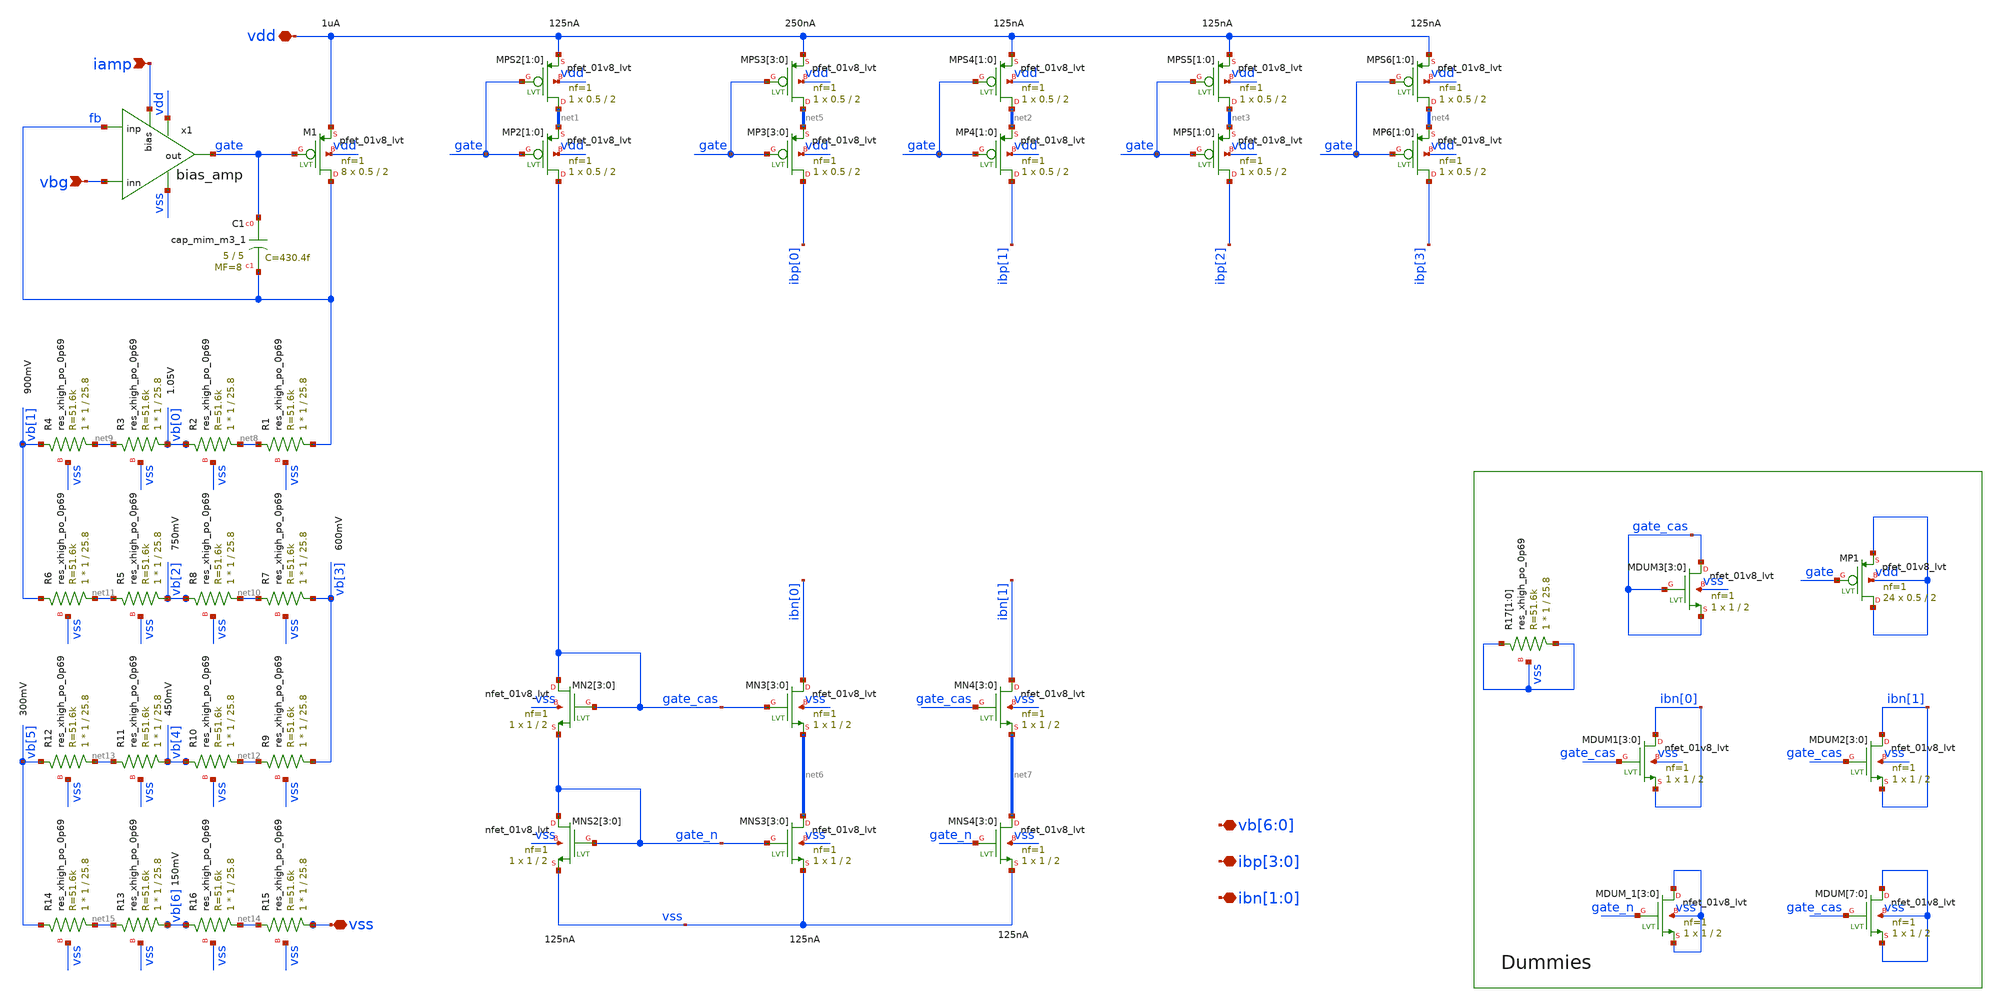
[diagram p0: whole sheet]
** sch_path: xschem/bias/bias.sch
**.subckt bias vbg iamp vdd ibp[3],ibp[2],ibp[1],ibp[0] ibn[1],ibn[0]
*+ vb[6],vb[5],vb[4],vb[3],vb[2],vb[1],vb[0] vss
*.ipin vbg
*.ipin iamp
*.iopin vdd
*.iopin ibp[3],ibp[2],ibp[1],ibp[0]
*.iopin ibn[1],ibn[0]
*.iopin vb[6],vb[5],vb[4],vb[3],vb[2],vb[1],vb[0]
*.iopin vss
x1 vdd gate fb vbg vss iamp bias_amp
XMP2[1] gate_cas gate net1[1] vdd sky130_fd_pr__pfet_01v8_lvt L=2 W=0.5 nf=1 ad='int((nf+1)/2) * W/nf * 0.29'
+ as='int((nf+2)/2) * W/nf * 0.29' pd='2*int((nf+1)/2) * (W/nf + 0.29)' ps='2*int((nf+2)/2) * (W/nf + 0.29)'
+ nrd='0.29 / W' nrs='0.29 / W' sa=0 sb=0 sd=0 mult=1 m=1
XMP2[0] gate_cas gate net1[0] vdd sky130_fd_pr__pfet_01v8_lvt L=2 W=0.5 nf=1 ad='int((nf+1)/2) * W/nf * 0.29'
+ as='int((nf+2)/2) * W/nf * 0.29' pd='2*int((nf+1)/2) * (W/nf + 0.29)' ps='2*int((nf+2)/2) * (W/nf + 0.29)'
+ nrd='0.29 / W' nrs='0.29 / W' sa=0 sb=0 sd=0 mult=1 m=1
XM1 fb gate vdd vdd sky130_fd_pr__pfet_01v8_lvt L=2 W=0.5 nf=1 ad='int((nf+1)/2) * W/nf * 0.29' as='int((nf+2)/2) * W/nf * 0.29'
+ pd='2*int((nf+1)/2) * (W/nf + 0.29)' ps='2*int((nf+2)/2) * (W/nf + 0.29)' nrd='0.29 / W' nrs='0.29 / W'
+ sa=0 sb=0 sd=0 mult=8 m=8
XMPS2[1] net1[1] gate vdd vdd sky130_fd_pr__pfet_01v8_lvt L=2 W=0.5 nf=1 ad='int((nf+1)/2) * W/nf * 0.29'
+ as='int((nf+2)/2) * W/nf * 0.29' pd='2*int((nf+1)/2) * (W/nf + 0.29)' ps='2*int((nf+2)/2) * (W/nf + 0.29)'
+ nrd='0.29 / W' nrs='0.29 / W' sa=0 sb=0 sd=0 mult=1 m=1
XMPS2[0] net1[0] gate vdd vdd sky130_fd_pr__pfet_01v8_lvt L=2 W=0.5 nf=1 ad='int((nf+1)/2) * W/nf * 0.29'
+ as='int((nf+2)/2) * W/nf * 0.29' pd='2*int((nf+1)/2) * (W/nf + 0.29)' ps='2*int((nf+2)/2) * (W/nf + 0.29)'
+ nrd='0.29 / W' nrs='0.29 / W' sa=0 sb=0 sd=0 mult=1 m=1
XMP4[1] ibp[1] gate net2[1] vdd sky130_fd_pr__pfet_01v8_lvt L=2 W=0.5 nf=1 ad='int((nf+1)/2) * W/nf * 0.29'
+ as='int((nf+2)/2) * W/nf * 0.29' pd='2*int((nf+1)/2) * (W/nf + 0.29)' ps='2*int((nf+2)/2) * (W/nf + 0.29)'
+ nrd='0.29 / W' nrs='0.29 / W' sa=0 sb=0 sd=0 mult=1 m=1
XMP4[0] ibp[1] gate net2[0] vdd sky130_fd_pr__pfet_01v8_lvt L=2 W=0.5 nf=1 ad='int((nf+1)/2) * W/nf * 0.29'
+ as='int((nf+2)/2) * W/nf * 0.29' pd='2*int((nf+1)/2) * (W/nf + 0.29)' ps='2*int((nf+2)/2) * (W/nf + 0.29)'
+ nrd='0.29 / W' nrs='0.29 / W' sa=0 sb=0 sd=0 mult=1 m=1
XMPS4[1] net2[1] gate vdd vdd sky130_fd_pr__pfet_01v8_lvt L=2 W=0.5 nf=1 ad='int((nf+1)/2) * W/nf * 0.29'
+ as='int((nf+2)/2) * W/nf * 0.29' pd='2*int((nf+1)/2) * (W/nf + 0.29)' ps='2*int((nf+2)/2) * (W/nf + 0.29)'
+ nrd='0.29 / W' nrs='0.29 / W' sa=0 sb=0 sd=0 mult=1 m=1
XMPS4[0] net2[0] gate vdd vdd sky130_fd_pr__pfet_01v8_lvt L=2 W=0.5 nf=1 ad='int((nf+1)/2) * W/nf * 0.29'
+ as='int((nf+2)/2) * W/nf * 0.29' pd='2*int((nf+1)/2) * (W/nf + 0.29)' ps='2*int((nf+2)/2) * (W/nf + 0.29)'
+ nrd='0.29 / W' nrs='0.29 / W' sa=0 sb=0 sd=0 mult=1 m=1
XMP5[1] ibp[2] gate net3[1] vdd sky130_fd_pr__pfet_01v8_lvt L=2 W=0.5 nf=1 ad='int((nf+1)/2) * W/nf * 0.29'
+ as='int((nf+2)/2) * W/nf * 0.29' pd='2*int((nf+1)/2) * (W/nf + 0.29)' ps='2*int((nf+2)/2) * (W/nf + 0.29)'
+ nrd='0.29 / W' nrs='0.29 / W' sa=0 sb=0 sd=0 mult=1 m=1
XMP5[0] ibp[2] gate net3[0] vdd sky130_fd_pr__pfet_01v8_lvt L=2 W=0.5 nf=1 ad='int((nf+1)/2) * W/nf * 0.29'
+ as='int((nf+2)/2) * W/nf * 0.29' pd='2*int((nf+1)/2) * (W/nf + 0.29)' ps='2*int((nf+2)/2) * (W/nf + 0.29)'
+ nrd='0.29 / W' nrs='0.29 / W' sa=0 sb=0 sd=0 mult=1 m=1
XMPS5[1] net3[1] gate vdd vdd sky130_fd_pr__pfet_01v8_lvt L=2 W=0.5 nf=1 ad='int((nf+1)/2) * W/nf * 0.29'
+ as='int((nf+2)/2) * W/nf * 0.29' pd='2*int((nf+1)/2) * (W/nf + 0.29)' ps='2*int((nf+2)/2) * (W/nf + 0.29)'
+ nrd='0.29 / W' nrs='0.29 / W' sa=0 sb=0 sd=0 mult=1 m=1
XMPS5[0] net3[0] gate vdd vdd sky130_fd_pr__pfet_01v8_lvt L=2 W=0.5 nf=1 ad='int((nf+1)/2) * W/nf * 0.29'
+ as='int((nf+2)/2) * W/nf * 0.29' pd='2*int((nf+1)/2) * (W/nf + 0.29)' ps='2*int((nf+2)/2) * (W/nf + 0.29)'
+ nrd='0.29 / W' nrs='0.29 / W' sa=0 sb=0 sd=0 mult=1 m=1
XMP6[1] ibp[3] gate net4[1] vdd sky130_fd_pr__pfet_01v8_lvt L=2 W=0.5 nf=1 ad='int((nf+1)/2) * W/nf * 0.29'
+ as='int((nf+2)/2) * W/nf * 0.29' pd='2*int((nf+1)/2) * (W/nf + 0.29)' ps='2*int((nf+2)/2) * (W/nf + 0.29)'
+ nrd='0.29 / W' nrs='0.29 / W' sa=0 sb=0 sd=0 mult=1 m=1
XMP6[0] ibp[3] gate net4[0] vdd sky130_fd_pr__pfet_01v8_lvt L=2 W=0.5 nf=1 ad='int((nf+1)/2) * W/nf * 0.29'
+ as='int((nf+2)/2) * W/nf * 0.29' pd='2*int((nf+1)/2) * (W/nf + 0.29)' ps='2*int((nf+2)/2) * (W/nf + 0.29)'
+ nrd='0.29 / W' nrs='0.29 / W' sa=0 sb=0 sd=0 mult=1 m=1
XMPS6[1] net4[1] gate vdd vdd sky130_fd_pr__pfet_01v8_lvt L=2 W=0.5 nf=1 ad='int((nf+1)/2) * W/nf * 0.29'
+ as='int((nf+2)/2) * W/nf * 0.29' pd='2*int((nf+1)/2) * (W/nf + 0.29)' ps='2*int((nf+2)/2) * (W/nf + 0.29)'
+ nrd='0.29 / W' nrs='0.29 / W' sa=0 sb=0 sd=0 mult=1 m=1
XMPS6[0] net4[0] gate vdd vdd sky130_fd_pr__pfet_01v8_lvt L=2 W=0.5 nf=1 ad='int((nf+1)/2) * W/nf * 0.29'
+ as='int((nf+2)/2) * W/nf * 0.29' pd='2*int((nf+1)/2) * (W/nf + 0.29)' ps='2*int((nf+2)/2) * (W/nf + 0.29)'
+ nrd='0.29 / W' nrs='0.29 / W' sa=0 sb=0 sd=0 mult=1 m=1
XMP3[3] ibp[0] gate net5[3] vdd sky130_fd_pr__pfet_01v8_lvt L=2 W=0.5 nf=1 ad='int((nf+1)/2) * W/nf * 0.29'
+ as='int((nf+2)/2) * W/nf * 0.29' pd='2*int((nf+1)/2) * (W/nf + 0.29)' ps='2*int((nf+2)/2) * (W/nf + 0.29)'
+ nrd='0.29 / W' nrs='0.29 / W' sa=0 sb=0 sd=0 mult=1 m=1
XMP3[2] ibp[0] gate net5[2] vdd sky130_fd_pr__pfet_01v8_lvt L=2 W=0.5 nf=1 ad='int((nf+1)/2) * W/nf * 0.29'
+ as='int((nf+2)/2) * W/nf * 0.29' pd='2*int((nf+1)/2) * (W/nf + 0.29)' ps='2*int((nf+2)/2) * (W/nf + 0.29)'
+ nrd='0.29 / W' nrs='0.29 / W' sa=0 sb=0 sd=0 mult=1 m=1
XMP3[1] ibp[0] gate net5[1] vdd sky130_fd_pr__pfet_01v8_lvt L=2 W=0.5 nf=1 ad='int((nf+1)/2) * W/nf * 0.29'
+ as='int((nf+2)/2) * W/nf * 0.29' pd='2*int((nf+1)/2) * (W/nf + 0.29)' ps='2*int((nf+2)/2) * (W/nf + 0.29)'
+ nrd='0.29 / W' nrs='0.29 / W' sa=0 sb=0 sd=0 mult=1 m=1
XMP3[0] ibp[0] gate net5[0] vdd sky130_fd_pr__pfet_01v8_lvt L=2 W=0.5 nf=1 ad='int((nf+1)/2) * W/nf * 0.29'
+ as='int((nf+2)/2) * W/nf * 0.29' pd='2*int((nf+1)/2) * (W/nf + 0.29)' ps='2*int((nf+2)/2) * (W/nf + 0.29)'
+ nrd='0.29 / W' nrs='0.29 / W' sa=0 sb=0 sd=0 mult=1 m=1
XMPS3[3] net5[3] gate vdd vdd sky130_fd_pr__pfet_01v8_lvt L=2 W=0.5 nf=1 ad='int((nf+1)/2) * W/nf * 0.29'
+ as='int((nf+2)/2) * W/nf * 0.29' pd='2*int((nf+1)/2) * (W/nf + 0.29)' ps='2*int((nf+2)/2) * (W/nf + 0.29)'
+ nrd='0.29 / W' nrs='0.29 / W' sa=0 sb=0 sd=0 mult=1 m=1
XMPS3[2] net5[2] gate vdd vdd sky130_fd_pr__pfet_01v8_lvt L=2 W=0.5 nf=1 ad='int((nf+1)/2) * W/nf * 0.29'
+ as='int((nf+2)/2) * W/nf * 0.29' pd='2*int((nf+1)/2) * (W/nf + 0.29)' ps='2*int((nf+2)/2) * (W/nf + 0.29)'
+ nrd='0.29 / W' nrs='0.29 / W' sa=0 sb=0 sd=0 mult=1 m=1
XMPS3[1] net5[1] gate vdd vdd sky130_fd_pr__pfet_01v8_lvt L=2 W=0.5 nf=1 ad='int((nf+1)/2) * W/nf * 0.29'
+ as='int((nf+2)/2) * W/nf * 0.29' pd='2*int((nf+1)/2) * (W/nf + 0.29)' ps='2*int((nf+2)/2) * (W/nf + 0.29)'
+ nrd='0.29 / W' nrs='0.29 / W' sa=0 sb=0 sd=0 mult=1 m=1
XMPS3[0] net5[0] gate vdd vdd sky130_fd_pr__pfet_01v8_lvt L=2 W=0.5 nf=1 ad='int((nf+1)/2) * W/nf * 0.29'
+ as='int((nf+2)/2) * W/nf * 0.29' pd='2*int((nf+1)/2) * (W/nf + 0.29)' ps='2*int((nf+2)/2) * (W/nf + 0.29)'
+ nrd='0.29 / W' nrs='0.29 / W' sa=0 sb=0 sd=0 mult=1 m=1
XMNS2[3] gate_n gate_n vss vss sky130_fd_pr__nfet_01v8_lvt L=2 W=1 nf=1 ad='int((nf+1)/2) * W/nf * 0.29'
+ as='int((nf+2)/2) * W/nf * 0.29' pd='2*int((nf+1)/2) * (W/nf + 0.29)' ps='2*int((nf+2)/2) * (W/nf + 0.29)'
+ nrd='0.29 / W' nrs='0.29 / W' sa=0 sb=0 sd=0 mult=1 m=1
XMNS2[2] gate_n gate_n vss vss sky130_fd_pr__nfet_01v8_lvt L=2 W=1 nf=1 ad='int((nf+1)/2) * W/nf * 0.29'
+ as='int((nf+2)/2) * W/nf * 0.29' pd='2*int((nf+1)/2) * (W/nf + 0.29)' ps='2*int((nf+2)/2) * (W/nf + 0.29)'
+ nrd='0.29 / W' nrs='0.29 / W' sa=0 sb=0 sd=0 mult=1 m=1
XMNS2[1] gate_n gate_n vss vss sky130_fd_pr__nfet_01v8_lvt L=2 W=1 nf=1 ad='int((nf+1)/2) * W/nf * 0.29'
+ as='int((nf+2)/2) * W/nf * 0.29' pd='2*int((nf+1)/2) * (W/nf + 0.29)' ps='2*int((nf+2)/2) * (W/nf + 0.29)'
+ nrd='0.29 / W' nrs='0.29 / W' sa=0 sb=0 sd=0 mult=1 m=1
XMNS2[0] gate_n gate_n vss vss sky130_fd_pr__nfet_01v8_lvt L=2 W=1 nf=1 ad='int((nf+1)/2) * W/nf * 0.29'
+ as='int((nf+2)/2) * W/nf * 0.29' pd='2*int((nf+1)/2) * (W/nf + 0.29)' ps='2*int((nf+2)/2) * (W/nf + 0.29)'
+ nrd='0.29 / W' nrs='0.29 / W' sa=0 sb=0 sd=0 mult=1 m=1
XMNS3[3] net6[3] gate_n vss vss sky130_fd_pr__nfet_01v8_lvt L=2 W=1 nf=1 ad='int((nf+1)/2) * W/nf * 0.29'
+ as='int((nf+2)/2) * W/nf * 0.29' pd='2*int((nf+1)/2) * (W/nf + 0.29)' ps='2*int((nf+2)/2) * (W/nf + 0.29)'
+ nrd='0.29 / W' nrs='0.29 / W' sa=0 sb=0 sd=0 mult=1 m=1
XMNS3[2] net6[2] gate_n vss vss sky130_fd_pr__nfet_01v8_lvt L=2 W=1 nf=1 ad='int((nf+1)/2) * W/nf * 0.29'
+ as='int((nf+2)/2) * W/nf * 0.29' pd='2*int((nf+1)/2) * (W/nf + 0.29)' ps='2*int((nf+2)/2) * (W/nf + 0.29)'
+ nrd='0.29 / W' nrs='0.29 / W' sa=0 sb=0 sd=0 mult=1 m=1
XMNS3[1] net6[1] gate_n vss vss sky130_fd_pr__nfet_01v8_lvt L=2 W=1 nf=1 ad='int((nf+1)/2) * W/nf * 0.29'
+ as='int((nf+2)/2) * W/nf * 0.29' pd='2*int((nf+1)/2) * (W/nf + 0.29)' ps='2*int((nf+2)/2) * (W/nf + 0.29)'
+ nrd='0.29 / W' nrs='0.29 / W' sa=0 sb=0 sd=0 mult=1 m=1
XMNS3[0] net6[0] gate_n vss vss sky130_fd_pr__nfet_01v8_lvt L=2 W=1 nf=1 ad='int((nf+1)/2) * W/nf * 0.29'
+ as='int((nf+2)/2) * W/nf * 0.29' pd='2*int((nf+1)/2) * (W/nf + 0.29)' ps='2*int((nf+2)/2) * (W/nf + 0.29)'
+ nrd='0.29 / W' nrs='0.29 / W' sa=0 sb=0 sd=0 mult=1 m=1
XMNS4[3] net7[3] gate_n vss vss sky130_fd_pr__nfet_01v8_lvt L=2 W=1 nf=1 ad='int((nf+1)/2) * W/nf * 0.29'
+ as='int((nf+2)/2) * W/nf * 0.29' pd='2*int((nf+1)/2) * (W/nf + 0.29)' ps='2*int((nf+2)/2) * (W/nf + 0.29)'
+ nrd='0.29 / W' nrs='0.29 / W' sa=0 sb=0 sd=0 mult=1 m=1
XMNS4[2] net7[2] gate_n vss vss sky130_fd_pr__nfet_01v8_lvt L=2 W=1 nf=1 ad='int((nf+1)/2) * W/nf * 0.29'
+ as='int((nf+2)/2) * W/nf * 0.29' pd='2*int((nf+1)/2) * (W/nf + 0.29)' ps='2*int((nf+2)/2) * (W/nf + 0.29)'
+ nrd='0.29 / W' nrs='0.29 / W' sa=0 sb=0 sd=0 mult=1 m=1
XMNS4[1] net7[1] gate_n vss vss sky130_fd_pr__nfet_01v8_lvt L=2 W=1 nf=1 ad='int((nf+1)/2) * W/nf * 0.29'
+ as='int((nf+2)/2) * W/nf * 0.29' pd='2*int((nf+1)/2) * (W/nf + 0.29)' ps='2*int((nf+2)/2) * (W/nf + 0.29)'
+ nrd='0.29 / W' nrs='0.29 / W' sa=0 sb=0 sd=0 mult=1 m=1
XMNS4[0] net7[0] gate_n vss vss sky130_fd_pr__nfet_01v8_lvt L=2 W=1 nf=1 ad='int((nf+1)/2) * W/nf * 0.29'
+ as='int((nf+2)/2) * W/nf * 0.29' pd='2*int((nf+1)/2) * (W/nf + 0.29)' ps='2*int((nf+2)/2) * (W/nf + 0.29)'
+ nrd='0.29 / W' nrs='0.29 / W' sa=0 sb=0 sd=0 mult=1 m=1
XMN2[3] gate_cas gate_cas gate_n vss sky130_fd_pr__nfet_01v8_lvt L=2 W=1 nf=1 ad='int((nf+1)/2) * W/nf * 0.29'
+ as='int((nf+2)/2) * W/nf * 0.29' pd='2*int((nf+1)/2) * (W/nf + 0.29)' ps='2*int((nf+2)/2) * (W/nf + 0.29)'
+ nrd='0.29 / W' nrs='0.29 / W' sa=0 sb=0 sd=0 mult=1 m=1
XMN2[2] gate_cas gate_cas gate_n vss sky130_fd_pr__nfet_01v8_lvt L=2 W=1 nf=1 ad='int((nf+1)/2) * W/nf * 0.29'
+ as='int((nf+2)/2) * W/nf * 0.29' pd='2*int((nf+1)/2) * (W/nf + 0.29)' ps='2*int((nf+2)/2) * (W/nf + 0.29)'
+ nrd='0.29 / W' nrs='0.29 / W' sa=0 sb=0 sd=0 mult=1 m=1
XMN2[1] gate_cas gate_cas gate_n vss sky130_fd_pr__nfet_01v8_lvt L=2 W=1 nf=1 ad='int((nf+1)/2) * W/nf * 0.29'
+ as='int((nf+2)/2) * W/nf * 0.29' pd='2*int((nf+1)/2) * (W/nf + 0.29)' ps='2*int((nf+2)/2) * (W/nf + 0.29)'
+ nrd='0.29 / W' nrs='0.29 / W' sa=0 sb=0 sd=0 mult=1 m=1
XMN2[0] gate_cas gate_cas gate_n vss sky130_fd_pr__nfet_01v8_lvt L=2 W=1 nf=1 ad='int((nf+1)/2) * W/nf * 0.29'
+ as='int((nf+2)/2) * W/nf * 0.29' pd='2*int((nf+1)/2) * (W/nf + 0.29)' ps='2*int((nf+2)/2) * (W/nf + 0.29)'
+ nrd='0.29 / W' nrs='0.29 / W' sa=0 sb=0 sd=0 mult=1 m=1
XMN3[3] ibn[0] gate_cas net6[3] vss sky130_fd_pr__nfet_01v8_lvt L=2 W=1 nf=1 ad='int((nf+1)/2) * W/nf * 0.29'
+ as='int((nf+2)/2) * W/nf * 0.29' pd='2*int((nf+1)/2) * (W/nf + 0.29)' ps='2*int((nf+2)/2) * (W/nf + 0.29)'
+ nrd='0.29 / W' nrs='0.29 / W' sa=0 sb=0 sd=0 mult=1 m=1
XMN3[2] ibn[0] gate_cas net6[2] vss sky130_fd_pr__nfet_01v8_lvt L=2 W=1 nf=1 ad='int((nf+1)/2) * W/nf * 0.29'
+ as='int((nf+2)/2) * W/nf * 0.29' pd='2*int((nf+1)/2) * (W/nf + 0.29)' ps='2*int((nf+2)/2) * (W/nf + 0.29)'
+ nrd='0.29 / W' nrs='0.29 / W' sa=0 sb=0 sd=0 mult=1 m=1
XMN3[1] ibn[0] gate_cas net6[1] vss sky130_fd_pr__nfet_01v8_lvt L=2 W=1 nf=1 ad='int((nf+1)/2) * W/nf * 0.29'
+ as='int((nf+2)/2) * W/nf * 0.29' pd='2*int((nf+1)/2) * (W/nf + 0.29)' ps='2*int((nf+2)/2) * (W/nf + 0.29)'
+ nrd='0.29 / W' nrs='0.29 / W' sa=0 sb=0 sd=0 mult=1 m=1
XMN3[0] ibn[0] gate_cas net6[0] vss sky130_fd_pr__nfet_01v8_lvt L=2 W=1 nf=1 ad='int((nf+1)/2) * W/nf * 0.29'
+ as='int((nf+2)/2) * W/nf * 0.29' pd='2*int((nf+1)/2) * (W/nf + 0.29)' ps='2*int((nf+2)/2) * (W/nf + 0.29)'
+ nrd='0.29 / W' nrs='0.29 / W' sa=0 sb=0 sd=0 mult=1 m=1
XMN4[3] ibn[1] gate_cas net7[3] vss sky130_fd_pr__nfet_01v8_lvt L=2 W=1 nf=1 ad='int((nf+1)/2) * W/nf * 0.29'
+ as='int((nf+2)/2) * W/nf * 0.29' pd='2*int((nf+1)/2) * (W/nf + 0.29)' ps='2*int((nf+2)/2) * (W/nf + 0.29)'
+ nrd='0.29 / W' nrs='0.29 / W' sa=0 sb=0 sd=0 mult=1 m=1
XMN4[2] ibn[1] gate_cas net7[2] vss sky130_fd_pr__nfet_01v8_lvt L=2 W=1 nf=1 ad='int((nf+1)/2) * W/nf * 0.29'
+ as='int((nf+2)/2) * W/nf * 0.29' pd='2*int((nf+1)/2) * (W/nf + 0.29)' ps='2*int((nf+2)/2) * (W/nf + 0.29)'
+ nrd='0.29 / W' nrs='0.29 / W' sa=0 sb=0 sd=0 mult=1 m=1
XMN4[1] ibn[1] gate_cas net7[1] vss sky130_fd_pr__nfet_01v8_lvt L=2 W=1 nf=1 ad='int((nf+1)/2) * W/nf * 0.29'
+ as='int((nf+2)/2) * W/nf * 0.29' pd='2*int((nf+1)/2) * (W/nf + 0.29)' ps='2*int((nf+2)/2) * (W/nf + 0.29)'
+ nrd='0.29 / W' nrs='0.29 / W' sa=0 sb=0 sd=0 mult=1 m=1
XMN4[0] ibn[1] gate_cas net7[0] vss sky130_fd_pr__nfet_01v8_lvt L=2 W=1 nf=1 ad='int((nf+1)/2) * W/nf * 0.29'
+ as='int((nf+2)/2) * W/nf * 0.29' pd='2*int((nf+1)/2) * (W/nf + 0.29)' ps='2*int((nf+2)/2) * (W/nf + 0.29)'
+ nrd='0.29 / W' nrs='0.29 / W' sa=0 sb=0 sd=0 mult=1 m=1
XC1 gate fb sky130_fd_pr__cap_mim_m3_1 W=5 L=5 MF=8 m=8
XR1 fb net8 vss sky130_fd_pr__res_xhigh_po_0p69 W=1 L=25.8 mult=1 m=1
XR2 net8 vb[0] vss sky130_fd_pr__res_xhigh_po_0p69 W=1 L=25.8 mult=1 m=1
XR3 vb[0] net9 vss sky130_fd_pr__res_xhigh_po_0p69 W=1 L=25.8 mult=1 m=1
XR4 net9 vb[1] vss sky130_fd_pr__res_xhigh_po_0p69 W=1 L=25.8 mult=1 m=1
XR5 vb[2] net11 vss sky130_fd_pr__res_xhigh_po_0p69 W=1 L=25.8 mult=1 m=1
XR6 net11 vb[1] vss sky130_fd_pr__res_xhigh_po_0p69 W=1 L=25.8 mult=1 m=1
XR7 vb[3] net10 vss sky130_fd_pr__res_xhigh_po_0p69 W=1 L=25.8 mult=1 m=1
XR8 net10 vb[2] vss sky130_fd_pr__res_xhigh_po_0p69 W=1 L=25.8 mult=1 m=1
XR9 vb[3] net12 vss sky130_fd_pr__res_xhigh_po_0p69 W=1 L=25.8 mult=1 m=1
XR10 net12 vb[4] vss sky130_fd_pr__res_xhigh_po_0p69 W=1 L=25.8 mult=1 m=1
XR11 vb[4] net13 vss sky130_fd_pr__res_xhigh_po_0p69 W=1 L=25.8 mult=1 m=1
XR12 net13 vb[5] vss sky130_fd_pr__res_xhigh_po_0p69 W=1 L=25.8 mult=1 m=1
XR13 vb[6] net15 vss sky130_fd_pr__res_xhigh_po_0p69 W=1 L=25.8 mult=1 m=1
XR14 net15 vb[5] vss sky130_fd_pr__res_xhigh_po_0p69 W=1 L=25.8 mult=1 m=1
XR15 vss net14 vss sky130_fd_pr__res_xhigh_po_0p69 W=1 L=25.8 mult=1 m=1
XR16 net14 vb[6] vss sky130_fd_pr__res_xhigh_po_0p69 W=1 L=25.8 mult=1 m=1
XMP1 vdd gate vdd vdd sky130_fd_pr__pfet_01v8_lvt L=2 W=0.5 nf=1 ad='int((nf+1)/2) * W/nf * 0.29' as='int((nf+2)/2) * W/nf * 0.29'
+ pd='2*int((nf+1)/2) * (W/nf + 0.29)' ps='2*int((nf+2)/2) * (W/nf + 0.29)' nrd='0.29 / W' nrs='0.29 / W'
+ sa=0 sb=0 sd=0 mult=24 m=24
XMDUM[7] vss gate_cas vss vss sky130_fd_pr__nfet_01v8_lvt L=2 W=1 nf=1 ad='int((nf+1)/2) * W/nf * 0.29'
+ as='int((nf+2)/2) * W/nf * 0.29' pd='2*int((nf+1)/2) * (W/nf + 0.29)' ps='2*int((nf+2)/2) * (W/nf + 0.29)'
+ nrd='0.29 / W' nrs='0.29 / W' sa=0 sb=0 sd=0 mult=1 m=1
XMDUM[6] vss gate_cas vss vss sky130_fd_pr__nfet_01v8_lvt L=2 W=1 nf=1 ad='int((nf+1)/2) * W/nf * 0.29'
+ as='int((nf+2)/2) * W/nf * 0.29' pd='2*int((nf+1)/2) * (W/nf + 0.29)' ps='2*int((nf+2)/2) * (W/nf + 0.29)'
+ nrd='0.29 / W' nrs='0.29 / W' sa=0 sb=0 sd=0 mult=1 m=1
XMDUM[5] vss gate_cas vss vss sky130_fd_pr__nfet_01v8_lvt L=2 W=1 nf=1 ad='int((nf+1)/2) * W/nf * 0.29'
+ as='int((nf+2)/2) * W/nf * 0.29' pd='2*int((nf+1)/2) * (W/nf + 0.29)' ps='2*int((nf+2)/2) * (W/nf + 0.29)'
+ nrd='0.29 / W' nrs='0.29 / W' sa=0 sb=0 sd=0 mult=1 m=1
XMDUM[4] vss gate_cas vss vss sky130_fd_pr__nfet_01v8_lvt L=2 W=1 nf=1 ad='int((nf+1)/2) * W/nf * 0.29'
+ as='int((nf+2)/2) * W/nf * 0.29' pd='2*int((nf+1)/2) * (W/nf + 0.29)' ps='2*int((nf+2)/2) * (W/nf + 0.29)'
+ nrd='0.29 / W' nrs='0.29 / W' sa=0 sb=0 sd=0 mult=1 m=1
XMDUM[3] vss gate_cas vss vss sky130_fd_pr__nfet_01v8_lvt L=2 W=1 nf=1 ad='int((nf+1)/2) * W/nf * 0.29'
+ as='int((nf+2)/2) * W/nf * 0.29' pd='2*int((nf+1)/2) * (W/nf + 0.29)' ps='2*int((nf+2)/2) * (W/nf + 0.29)'
+ nrd='0.29 / W' nrs='0.29 / W' sa=0 sb=0 sd=0 mult=1 m=1
XMDUM[2] vss gate_cas vss vss sky130_fd_pr__nfet_01v8_lvt L=2 W=1 nf=1 ad='int((nf+1)/2) * W/nf * 0.29'
+ as='int((nf+2)/2) * W/nf * 0.29' pd='2*int((nf+1)/2) * (W/nf + 0.29)' ps='2*int((nf+2)/2) * (W/nf + 0.29)'
+ nrd='0.29 / W' nrs='0.29 / W' sa=0 sb=0 sd=0 mult=1 m=1
XMDUM[1] vss gate_cas vss vss sky130_fd_pr__nfet_01v8_lvt L=2 W=1 nf=1 ad='int((nf+1)/2) * W/nf * 0.29'
+ as='int((nf+2)/2) * W/nf * 0.29' pd='2*int((nf+1)/2) * (W/nf + 0.29)' ps='2*int((nf+2)/2) * (W/nf + 0.29)'
+ nrd='0.29 / W' nrs='0.29 / W' sa=0 sb=0 sd=0 mult=1 m=1
XMDUM[0] vss gate_cas vss vss sky130_fd_pr__nfet_01v8_lvt L=2 W=1 nf=1 ad='int((nf+1)/2) * W/nf * 0.29'
+ as='int((nf+2)/2) * W/nf * 0.29' pd='2*int((nf+1)/2) * (W/nf + 0.29)' ps='2*int((nf+2)/2) * (W/nf + 0.29)'
+ nrd='0.29 / W' nrs='0.29 / W' sa=0 sb=0 sd=0 mult=1 m=1
XMDUM_1[3] vss gate_n vss vss sky130_fd_pr__nfet_01v8_lvt L=2 W=1 nf=1 ad='int((nf+1)/2) * W/nf * 0.29'
+ as='int((nf+2)/2) * W/nf * 0.29' pd='2*int((nf+1)/2) * (W/nf + 0.29)' ps='2*int((nf+2)/2) * (W/nf + 0.29)'
+ nrd='0.29 / W' nrs='0.29 / W' sa=0 sb=0 sd=0 mult=1 m=1
XMDUM_1[2] vss gate_n vss vss sky130_fd_pr__nfet_01v8_lvt L=2 W=1 nf=1 ad='int((nf+1)/2) * W/nf * 0.29'
+ as='int((nf+2)/2) * W/nf * 0.29' pd='2*int((nf+1)/2) * (W/nf + 0.29)' ps='2*int((nf+2)/2) * (W/nf + 0.29)'
+ nrd='0.29 / W' nrs='0.29 / W' sa=0 sb=0 sd=0 mult=1 m=1
XMDUM_1[1] vss gate_n vss vss sky130_fd_pr__nfet_01v8_lvt L=2 W=1 nf=1 ad='int((nf+1)/2) * W/nf * 0.29'
+ as='int((nf+2)/2) * W/nf * 0.29' pd='2*int((nf+1)/2) * (W/nf + 0.29)' ps='2*int((nf+2)/2) * (W/nf + 0.29)'
+ nrd='0.29 / W' nrs='0.29 / W' sa=0 sb=0 sd=0 mult=1 m=1
XMDUM_1[0] vss gate_n vss vss sky130_fd_pr__nfet_01v8_lvt L=2 W=1 nf=1 ad='int((nf+1)/2) * W/nf * 0.29'
+ as='int((nf+2)/2) * W/nf * 0.29' pd='2*int((nf+1)/2) * (W/nf + 0.29)' ps='2*int((nf+2)/2) * (W/nf + 0.29)'
+ nrd='0.29 / W' nrs='0.29 / W' sa=0 sb=0 sd=0 mult=1 m=1
XMDUM1[3] ibn[0] gate_cas ibn[0] vss sky130_fd_pr__nfet_01v8_lvt L=2 W=1 nf=1 ad='int((nf+1)/2) * W/nf * 0.29'
+ as='int((nf+2)/2) * W/nf * 0.29' pd='2*int((nf+1)/2) * (W/nf + 0.29)' ps='2*int((nf+2)/2) * (W/nf + 0.29)'
+ nrd='0.29 / W' nrs='0.29 / W' sa=0 sb=0 sd=0 mult=1 m=1
XMDUM1[2] ibn[0] gate_cas ibn[0] vss sky130_fd_pr__nfet_01v8_lvt L=2 W=1 nf=1 ad='int((nf+1)/2) * W/nf * 0.29'
+ as='int((nf+2)/2) * W/nf * 0.29' pd='2*int((nf+1)/2) * (W/nf + 0.29)' ps='2*int((nf+2)/2) * (W/nf + 0.29)'
+ nrd='0.29 / W' nrs='0.29 / W' sa=0 sb=0 sd=0 mult=1 m=1
XMDUM1[1] ibn[0] gate_cas ibn[0] vss sky130_fd_pr__nfet_01v8_lvt L=2 W=1 nf=1 ad='int((nf+1)/2) * W/nf * 0.29'
+ as='int((nf+2)/2) * W/nf * 0.29' pd='2*int((nf+1)/2) * (W/nf + 0.29)' ps='2*int((nf+2)/2) * (W/nf + 0.29)'
+ nrd='0.29 / W' nrs='0.29 / W' sa=0 sb=0 sd=0 mult=1 m=1
XMDUM1[0] ibn[0] gate_cas ibn[0] vss sky130_fd_pr__nfet_01v8_lvt L=2 W=1 nf=1 ad='int((nf+1)/2) * W/nf * 0.29'
+ as='int((nf+2)/2) * W/nf * 0.29' pd='2*int((nf+1)/2) * (W/nf + 0.29)' ps='2*int((nf+2)/2) * (W/nf + 0.29)'
+ nrd='0.29 / W' nrs='0.29 / W' sa=0 sb=0 sd=0 mult=1 m=1
XMDUM2[3] ibn[1] gate_cas ibn[1] vss sky130_fd_pr__nfet_01v8_lvt L=2 W=1 nf=1 ad='int((nf+1)/2) * W/nf * 0.29'
+ as='int((nf+2)/2) * W/nf * 0.29' pd='2*int((nf+1)/2) * (W/nf + 0.29)' ps='2*int((nf+2)/2) * (W/nf + 0.29)'
+ nrd='0.29 / W' nrs='0.29 / W' sa=0 sb=0 sd=0 mult=1 m=1
XMDUM2[2] ibn[1] gate_cas ibn[1] vss sky130_fd_pr__nfet_01v8_lvt L=2 W=1 nf=1 ad='int((nf+1)/2) * W/nf * 0.29'
+ as='int((nf+2)/2) * W/nf * 0.29' pd='2*int((nf+1)/2) * (W/nf + 0.29)' ps='2*int((nf+2)/2) * (W/nf + 0.29)'
+ nrd='0.29 / W' nrs='0.29 / W' sa=0 sb=0 sd=0 mult=1 m=1
XMDUM2[1] ibn[1] gate_cas ibn[1] vss sky130_fd_pr__nfet_01v8_lvt L=2 W=1 nf=1 ad='int((nf+1)/2) * W/nf * 0.29'
+ as='int((nf+2)/2) * W/nf * 0.29' pd='2*int((nf+1)/2) * (W/nf + 0.29)' ps='2*int((nf+2)/2) * (W/nf + 0.29)'
+ nrd='0.29 / W' nrs='0.29 / W' sa=0 sb=0 sd=0 mult=1 m=1
XMDUM2[0] ibn[1] gate_cas ibn[1] vss sky130_fd_pr__nfet_01v8_lvt L=2 W=1 nf=1 ad='int((nf+1)/2) * W/nf * 0.29'
+ as='int((nf+2)/2) * W/nf * 0.29' pd='2*int((nf+1)/2) * (W/nf + 0.29)' ps='2*int((nf+2)/2) * (W/nf + 0.29)'
+ nrd='0.29 / W' nrs='0.29 / W' sa=0 sb=0 sd=0 mult=1 m=1
XMDUM3[3] gate_cas gate_cas gate_cas vss sky130_fd_pr__nfet_01v8_lvt L=2 W=1 nf=1 ad='int((nf+1)/2) * W/nf * 0.29'
+ as='int((nf+2)/2) * W/nf * 0.29' pd='2*int((nf+1)/2) * (W/nf + 0.29)' ps='2*int((nf+2)/2) * (W/nf + 0.29)'
+ nrd='0.29 / W' nrs='0.29 / W' sa=0 sb=0 sd=0 mult=1 m=1
XMDUM3[2] gate_cas gate_cas gate_cas vss sky130_fd_pr__nfet_01v8_lvt L=2 W=1 nf=1 ad='int((nf+1)/2) * W/nf * 0.29'
+ as='int((nf+2)/2) * W/nf * 0.29' pd='2*int((nf+1)/2) * (W/nf + 0.29)' ps='2*int((nf+2)/2) * (W/nf + 0.29)'
+ nrd='0.29 / W' nrs='0.29 / W' sa=0 sb=0 sd=0 mult=1 m=1
XMDUM3[1] gate_cas gate_cas gate_cas vss sky130_fd_pr__nfet_01v8_lvt L=2 W=1 nf=1 ad='int((nf+1)/2) * W/nf * 0.29'
+ as='int((nf+2)/2) * W/nf * 0.29' pd='2*int((nf+1)/2) * (W/nf + 0.29)' ps='2*int((nf+2)/2) * (W/nf + 0.29)'
+ nrd='0.29 / W' nrs='0.29 / W' sa=0 sb=0 sd=0 mult=1 m=1
XMDUM3[0] gate_cas gate_cas gate_cas vss sky130_fd_pr__nfet_01v8_lvt L=2 W=1 nf=1 ad='int((nf+1)/2) * W/nf * 0.29'
+ as='int((nf+2)/2) * W/nf * 0.29' pd='2*int((nf+1)/2) * (W/nf + 0.29)' ps='2*int((nf+2)/2) * (W/nf + 0.29)'
+ nrd='0.29 / W' nrs='0.29 / W' sa=0 sb=0 sd=0 mult=1 m=1
XR17[1] vss vss vss sky130_fd_pr__res_xhigh_po_0p69 W=1 L=25.8 mult=1 m=1
XR17[0] vss vss vss sky130_fd_pr__res_xhigh_po_0p69 W=1 L=25.8 mult=1 m=1
**.ends

* expanding   symbol:  bias/bias_amp.sym # of pins=6
** sym_path: bias/bias_amp.sym
** sch_path: bias/bias_amp.sch
.subckt bias_amp vdd out inp inn vss bias
*.iopin vdd
*.iopin bias
*.ipin inp
*.ipin inn
*.opin out
*.iopin vss
XM3 mirr mirr vdd vdd sky130_fd_pr__pfet_01v8_lvt L=10 W=0.5 nf=1 ad='int((nf+1)/2) * W/nf * 0.29' as='int((nf+2)/2) * W/nf * 0.29'
+ pd='2*int((nf+1)/2) * (W/nf + 0.29)' ps='2*int((nf+2)/2) * (W/nf + 0.29)' nrd='0.29 / W' nrs='0.29 / W'
+ sa=0 sb=0 sd=0 mult=4 m=4
XM4 out mirr vdd vdd sky130_fd_pr__pfet_01v8_lvt L=10 W=0.5 nf=1 ad='int((nf+1)/2) * W/nf * 0.29' as='int((nf+2)/2) * W/nf * 0.29'
+ pd='2*int((nf+1)/2) * (W/nf + 0.29)' ps='2*int((nf+2)/2) * (W/nf + 0.29)' nrd='0.29 / W' nrs='0.29 / W'
+ sa=0 sb=0 sd=0 mult=4 m=4
XM1 mirr inp diff vss sky130_fd_pr__nfet_01v8_lvt L=8 W=0.5 nf=1 ad='int((nf+1)/2) * W/nf * 0.29' as='int((nf+2)/2) * W/nf * 0.29'
+ pd='2*int((nf+1)/2) * (W/nf + 0.29)' ps='2*int((nf+2)/2) * (W/nf + 0.29)' nrd='0.29 / W' nrs='0.29 / W'
+ sa=0 sb=0 sd=0 mult=4 m=4
XM2 out inn diff vss sky130_fd_pr__nfet_01v8_lvt L=8 W=0.5 nf=1 ad='int((nf+1)/2) * W/nf * 0.29' as='int((nf+2)/2) * W/nf * 0.29'
+ pd='2*int((nf+1)/2) * (W/nf + 0.29)' ps='2*int((nf+2)/2) * (W/nf + 0.29)' nrd='0.29 / W' nrs='0.29 / W'
+ sa=0 sb=0 sd=0 mult=4 m=4
XM5 net1 bias vss vss sky130_fd_pr__nfet_01v8_lvt L=4 W=0.5 nf=1 ad='int((nf+1)/2) * W/nf * 0.29' as='int((nf+2)/2) * W/nf * 0.29'
+ pd='2*int((nf+1)/2) * (W/nf + 0.29)' ps='2*int((nf+2)/2) * (W/nf + 0.29)' nrd='0.29 / W' nrs='0.29 / W'
+ sa=0 sb=0 sd=0 mult=4 m=4
XM6 bias bias vss vss sky130_fd_pr__nfet_01v8_lvt L=4 W=0.5 nf=1 ad='int((nf+1)/2) * W/nf * 0.29' as='int((nf+2)/2) * W/nf * 0.29'
+ pd='2*int((nf+1)/2) * (W/nf + 0.29)' ps='2*int((nf+2)/2) * (W/nf + 0.29)' nrd='0.29 / W' nrs='0.29 / W'
+ sa=0 sb=0 sd=0 mult=8 m=8
XM5s diff bias net1 vss sky130_fd_pr__nfet_01v8_lvt L=4 W=0.5 nf=1 ad='int((nf+1)/2) * W/nf * 0.29' as='int((nf+2)/2) * W/nf * 0.29'
+ pd='2*int((nf+1)/2) * (W/nf + 0.29)' ps='2*int((nf+2)/2) * (W/nf + 0.29)' nrd='0.29 / W' nrs='0.29 / W'
+ sa=0 sb=0 sd=0 mult=4 m=4
.ends

.end
